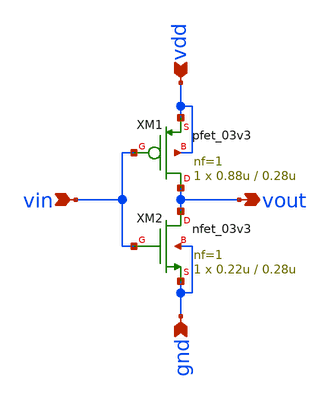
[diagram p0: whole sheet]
** sch_path: schem/inv_vtc.sch
**.subckt inv_vtc vin gnd vdd vout
*.ipin vin
*.ipin gnd
*.ipin vdd
*.opin vout
XM1 vout vin vdd vdd pfet_03v3 L=0.28u W=0.88u nf=1 ad='int((nf+1)/2) * W/nf * 0.18u' as='int((nf+2)/2) * W/nf * 0.18u'
+ pd='2*int((nf+1)/2) * (W/nf + 0.18u)' ps='2*int((nf+2)/2) * (W/nf + 0.18u)' nrd='0.18u / W' nrs='0.18u / W'
+ sa=0 sb=0 sd=0 m=1
XM2 vout vin gnd gnd nfet_03v3 L=0.28u W=0.22u nf=1 ad='int((nf+1)/2) * W/nf * 0.18u' as='int((nf+2)/2) * W/nf * 0.18u'
+ pd='2*int((nf+1)/2) * (W/nf + 0.18u)' ps='2*int((nf+2)/2) * (W/nf + 0.18u)' nrd='0.18u / W' nrs='0.18u / W'
+ sa=0 sb=0 sd=0 m=1
**.ends
.end
